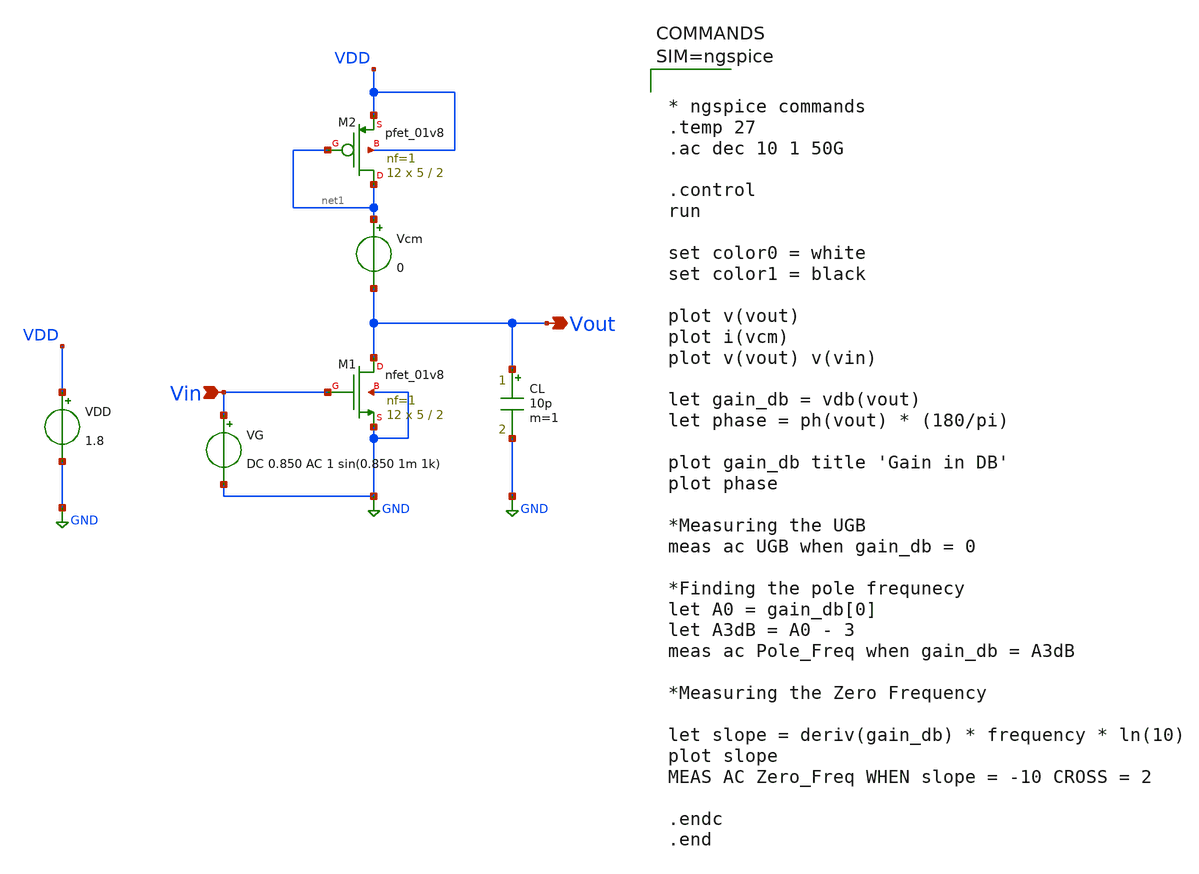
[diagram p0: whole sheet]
** sch_path: Common_Source_PMOS_Load_ckts/CS_Amp_PMOS_Diode_Load_Ckts/NMOS_PMOS_Diode_Load_AC_Analysis.sch
**.subckt NMOS_PMOS_Diode_Load_AC_Analysis Vout Vin
*.opin Vout
*.ipin Vin
XM1 Vout Vin GND GND sky130_fd_pr__nfet_01v8 L=2 W=5 nf=1 ad='int((1 + 1)/2) * 5 / 1 * 0.29' as='int((1 + 2)/2) * 5 / 1 * 0.29'
+ pd='2*int((1 + 1)/2) * (5 / 1 + 0.29)' ps='2*int((1 + 2)/2) * (5 / 1 + 0.29)' nrd='0.29 / 5 ' nrs='0.29 / 5 '
+ sa=0 sb=0 sd=0 mult=12 m=12
XM2 net1 net1 VDD VDD sky130_fd_pr__pfet_01v8 L=2 W=5 nf=1 ad='int((1 + 1)/2) * 5 / 1 * 0.29' as='int((1 + 2)/2) * 5 / 1 * 0.29'
+ pd='2*int((1 + 1)/2) * (5 / 1 + 0.29)' ps='2*int((1 + 2)/2) * (5 / 1 + 0.29)' nrd='0.29 / 5 ' nrs='0.29 / 5 '
+ sa=0 sb=0 sd=0 mult=12 m=12
Vcm net1 Vout 0
CL Vout GND 10p m=1
VG Vin GND DC 0.850 AC 1 sin(0.850 1m 1k)
VDD VDD GND 1.8
**** begin user architecture code

** opencircuitdesign pdks install
.lib $::SKYWATER_MODELS/sky130.lib.spice tt




* ngspice commands
.temp 27
.ac dec 10 1 50G

.control
run

set color0 = white
set color1 = black

plot v(vout)
plot i(vcm)
plot v(vout) v(vin)

let gain_db = vdb(vout)
let phase = ph(vout) * (180/pi)

plot gain_db title 'Gain in DB'
plot phase

*Measuring the UGB
meas ac UGB when gain_db = 0

*Finding the pole frequnecy
let A0 = gain_db[0]
let A3dB = A0 - 3
meas ac Pole_Freq when gain_db = A3dB

*Measuring the Zero Frequency

let slope = deriv(gain_db) * frequency * ln(10)
plot slope
MEAS AC Zero_Freq WHEN slope = -10 CROSS = 2

.endc
.end



**** end user architecture code
**.ends
.GLOBAL GND
.end
